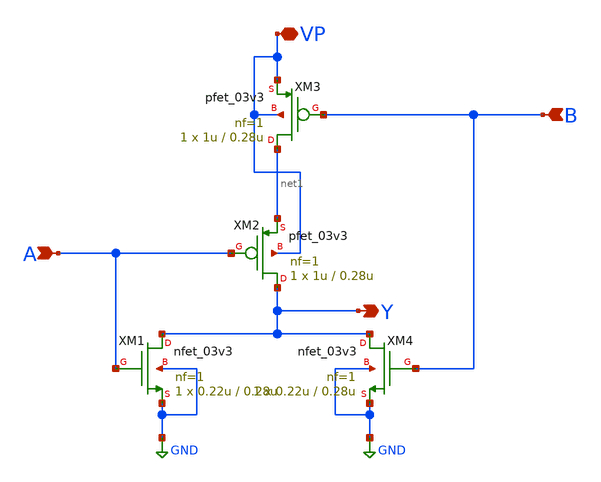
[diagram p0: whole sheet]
** sch_path: xschem/NOR2.sch
**.subckt NOR2 A B Y VP
*.ipin A
*.ipin B
*.opin Y
*.iopin VP
XM1 Y A GND GND nfet_03v3 L=0.28u W=0.22u nf=1 ad='int((nf+1)/2) * W/nf * 0.18u' as='int((nf+2)/2) * W/nf * 0.18u'
+ pd='2*int((nf+1)/2) * (W/nf + 0.18u)' ps='2*int((nf+2)/2) * (W/nf + 0.18u)' nrd='0.18u / W' nrs='0.18u / W'
+ sa=0 sb=0 sd=0 m=1
XM2 Y A net1 VP pfet_03v3 L=0.28u W=1u nf=1 ad='int((nf+1)/2) * W/nf * 0.18u' as='int((nf+2)/2) * W/nf * 0.18u'
+ pd='2*int((nf+1)/2) * (W/nf + 0.18u)' ps='2*int((nf+2)/2) * (W/nf + 0.18u)' nrd='0.18u / W' nrs='0.18u / W'
+ sa=0 sb=0 sd=0 m=1
XM4 Y B GND GND nfet_03v3 L=0.28u W=0.22u nf=1 ad='int((nf+1)/2) * W/nf * 0.18u' as='int((nf+2)/2) * W/nf * 0.18u'
+ pd='2*int((nf+1)/2) * (W/nf + 0.18u)' ps='2*int((nf+2)/2) * (W/nf + 0.18u)' nrd='0.18u / W' nrs='0.18u / W'
+ sa=0 sb=0 sd=0 m=1
XM3 net1 B VP VP pfet_03v3 L=0.28u W=1u nf=1 ad='int((nf+1)/2) * W/nf * 0.18u' as='int((nf+2)/2) * W/nf * 0.18u'
+ pd='2*int((nf+1)/2) * (W/nf + 0.18u)' ps='2*int((nf+2)/2) * (W/nf + 0.18u)' nrd='0.18u / W' nrs='0.18u / W'
+ sa=0 sb=0 sd=0 m=1
**.ends
.GLOBAL GND
.end
